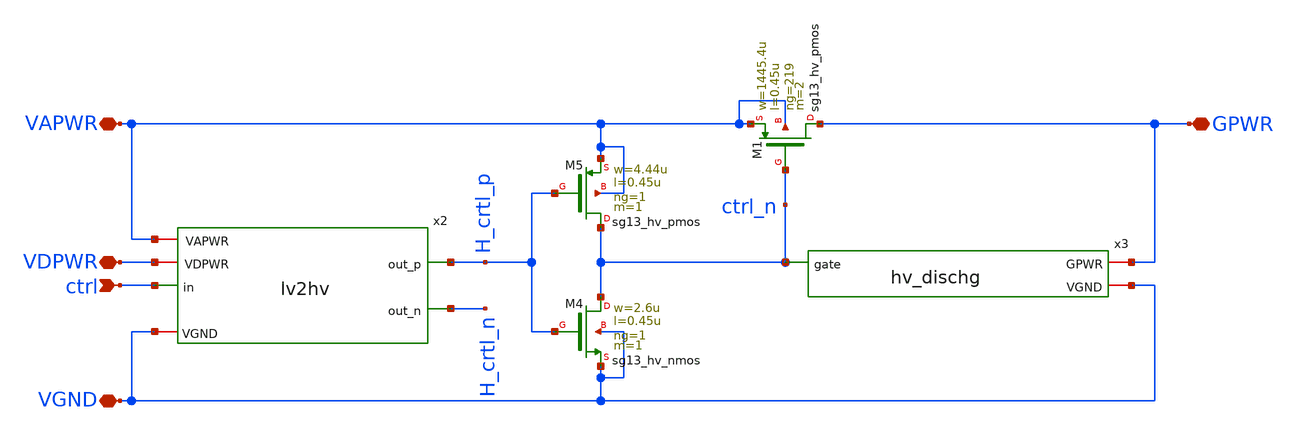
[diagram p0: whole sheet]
** sch_path: ihp-sg13cmos5l/libs.tech/xschem/hm_analog/hm_pg_hv.sch
**.subckt hm_pg_hv ctrl VAPWR VGND GPWR VDPWR
*.ipin ctrl
*.iopin VAPWR
*.iopin VGND
*.iopin GPWR
*.iopin VDPWR
x2 VAPWR VDPWR ctrl H_crtl_p H_crtl_n VGND lv2hv
XM4 ctrl_n H_crtl_p VGND VGND sg13_hv_nmos w=2.6u l=0.45u ng=1 m=1 mm_ok=1
XM5 ctrl_n H_crtl_p VAPWR VAPWR sg13_hv_pmos w=4.44u l=0.45u ng=1 m=1 mm_ok=1
XM1 GPWR ctrl_n VAPWR VAPWR sg13_hv_pmos w=1445.4u l=0.45u ng=219 m=2 mm_ok=1
x3 VGND GPWR ctrl_n hv_dischg
**.ends

* expanding   symbol:
*+  /foss/designs/hm-openpdk-library/ihp-sg13cmos5l/libs.tech/xschem/hm_analog/lv2hv.sym # of pins=6
** sym_path: ihp-sg13cmos5l/libs.tech/xschem/hm_analog/lv2hv.sym
** sch_path: ihp-sg13cmos5l/libs.tech/xschem/hm_analog/lv2hv.sch
.subckt lv2hv VAPWR VDPWR in out_p out_n VGND
*.iopin VAPWR
*.iopin VGND
*.ipin in
*.iopin VDPWR
*.opin out_p
*.opin out_n
XM1 in_n in VGND VGND sg13_lv_nmos w=1u l=0.13u ng=1 m=1 mm_ok=1
XM2 in_n in VDPWR VDPWR sg13_lv_pmos w=2u l=0.13u ng=1 m=1 mm_ok=1
XM3 in_p in_n VGND VGND sg13_lv_nmos w=1u l=0.13u ng=1 m=1 mm_ok=1
XM4 in_p in_n VDPWR VDPWR sg13_lv_pmos w=2u l=0.13u ng=1 m=1 mm_ok=1
XM5 out_p net1 VGND VGND sg13_hv_nmos w=1u l=0.45u ng=1 m=1 mm_ok=1
XM6 net1 in_p VGND VGND sg13_hv_nmos w=1u l=0.45u ng=1 m=1 mm_ok=1
XM7 out_p net1 VAPWR VAPWR sg13_hv_pmos w=2u l=0.45u ng=1 m=1 mm_ok=1
XM8 net1 net2 VAPWR VAPWR sg13_hv_pmos w=1u l=0.45u ng=1 m=1 mm_ok=1
XM9 net2 net1 VAPWR VAPWR sg13_hv_pmos w=1u l=0.45u ng=1 m=1 mm_ok=1
XM10 net2 in_n VGND VGND sg13_hv_nmos w=1u l=0.45u ng=1 m=1 mm_ok=1
XM11 out_n net2 VGND VGND sg13_hv_nmos w=1u l=0.45u ng=1 m=1 mm_ok=1
XM12 out_n net2 VAPWR VAPWR sg13_hv_pmos w=2u l=0.45u ng=1 m=1 mm_ok=1
.ends


* expanding   symbol:
*+  /foss/designs/hm-openpdk-library/ihp-sg13cmos5l/libs.tech/xschem/hm_analog/hv_dischg.sym # of pins=3
** sym_path: ihp-sg13cmos5l/libs.tech/xschem/hm_analog/hv_dischg.sym
** sch_path: ihp-sg13cmos5l/libs.tech/xschem/hm_analog/hv_dischg.sch
.subckt hv_dischg VGND GPWR gate
*.iopin GPWR
*.iopin VGND
*.ipin gate
XM6 GPWR gate net6 VGND sg13_hv_nmos w=0.5u l=0.65u ng=1 m=1 mm_ok=1
XM7 net6 gate net5 VGND sg13_hv_nmos w=0.5u l=0.65u ng=1 m=1 mm_ok=1
XM8 net5 gate net4 VGND sg13_hv_nmos w=0.5u l=0.65u ng=1 m=1 mm_ok=1
XM9 net4 gate VGND VGND sg13_hv_nmos w=0.5u l=0.65u ng=1 m=1 mm_ok=1
XM1 GPWR gate net1 VGND sg13_hv_nmos w=0.5u l=0.65u ng=1 m=1 mm_ok=1
XM2 net1 gate net2 VGND sg13_hv_nmos w=0.5u l=0.65u ng=1 m=1 mm_ok=1
XM3 net2 gate net3 VGND sg13_hv_nmos w=0.5u l=0.65u ng=1 m=1 mm_ok=1
XM4 net3 gate VGND VGND sg13_hv_nmos w=0.5u l=0.65u ng=1 m=1 mm_ok=1
.ends

.end
